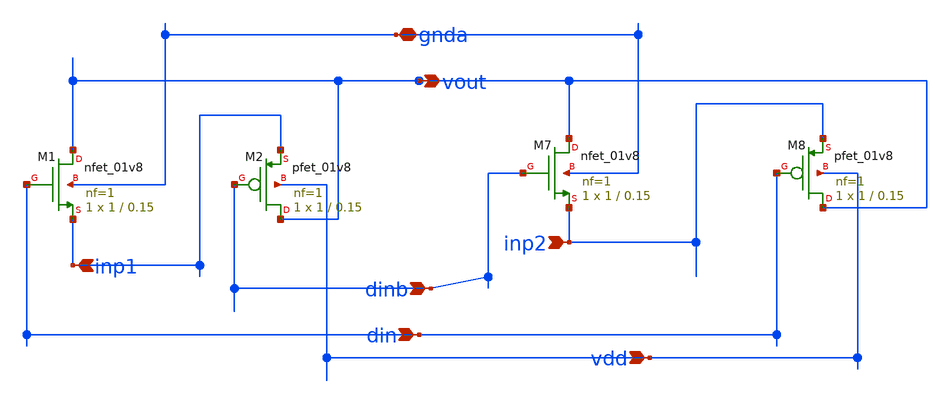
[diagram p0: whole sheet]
** sch_path: prelayout/TG2.sch
**.subckt TG2 din inp1 inp2 vdd vout gnda dinb
*.ipin din
*.ipin inp1
*.ipin inp2
*.ipin vdd
*.opin vout
*.iopin gnda
*.ipin dinb
XM1 vout din inp1 gnda sky130_fd_pr__nfet_01v8 L=0.15 W=1 nf=1 ad=0.3 as=0.3 pd=1.68 ps=1.68 nrd=0.3
+ nrs=0.3 sa=0 sb=0 sd=0 mult=1 m=1
XM2 vout dinb inp1 vdd sky130_fd_pr__pfet_01v8 L=0.15 W=1 nf=1 ad=0.3 as=0.3 pd=1.68 ps=1.68 nrd=0.3
+ nrs=0.3 sa=0 sb=0 sd=0 mult=1 m=1
XM7 vout dinb inp2 gnda sky130_fd_pr__nfet_01v8 L=0.15 W=1 nf=1 ad=0.3 as=0.3 pd=1.68 ps=1.68
+ nrd=0.3 nrs=0.3 sa=0 sb=0 sd=0 mult=1 m=1
XM8 vout din inp2 vdd sky130_fd_pr__pfet_01v8 L=0.15 W=1 nf=1 ad=0.3 as=0.3 pd=1.68 ps=1.68 nrd=0.3
+ nrs=0.3 sa=0 sb=0 sd=0 mult=1 m=1
**.ends
.end
